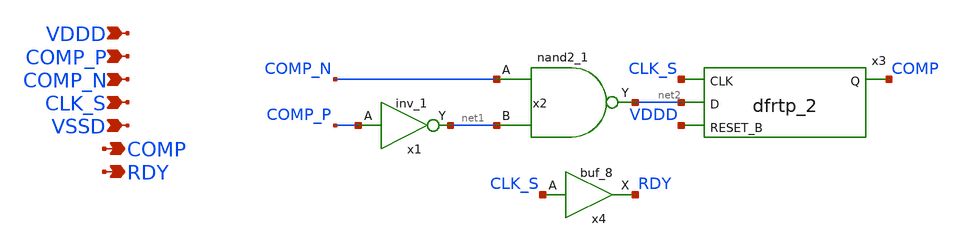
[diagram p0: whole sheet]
** sch_path: xschem/epc_value_processor.sch
**.subckt epc_value_processor COMP_P VDDD VSSD COMP RDY COMP_N CLK_S
*.ipin COMP_P
*.ipin VDDD
*.ipin VSSD
*.opin COMP
*.opin RDY
*.ipin COMP_N
*.ipin CLK_S
x1 COMP_P VSSD VSSD VDDD VDDD net1 sky130_fd_sc_hd__inv_1
x2 COMP_N net1 VSSD VSSD VDDD VDDD net2 sky130_fd_sc_hd__nand2_1
x3 CLK_S net2 VDDD VSSD VSSD VDDD VDDD COMP sky130_fd_sc_hd__dfrtp_2
x4 CLK_S VSSD VSSD VDDD VDDD RDY sky130_fd_sc_hd__buf_8
**.ends
.end
